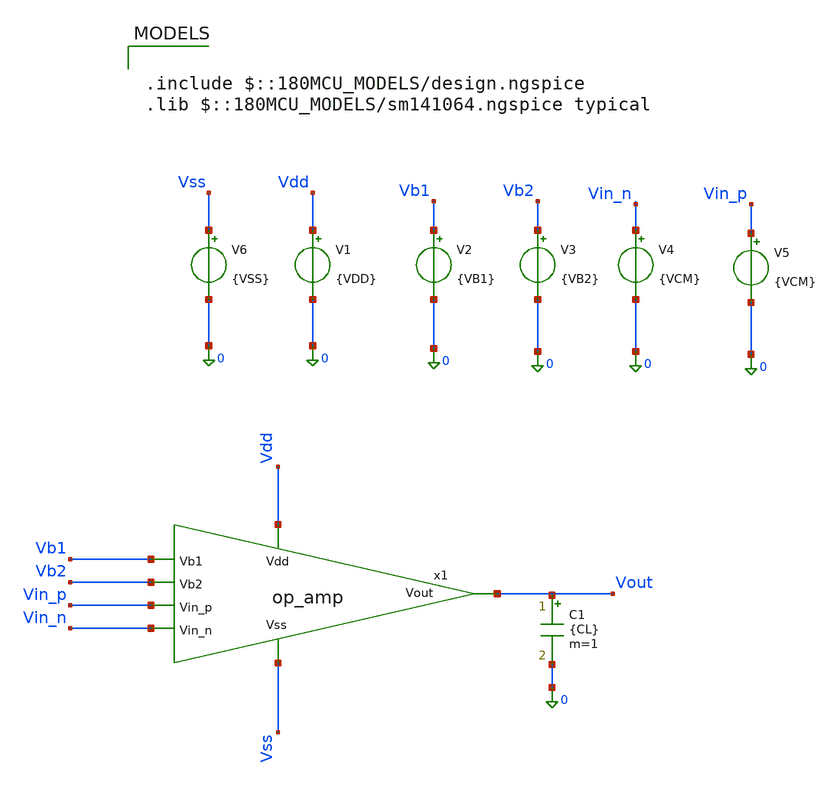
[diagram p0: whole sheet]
** sch_path: blocks/adc/lvds/ota_test.sch
**.subckt ota_test
C1 net1 0 {CL} m=1
V1 Vdd 0 {VDD}
V2 Vb1 0 {VB1}
V3 Vb2 0 {VB2}
V4 Vin_n 0 {VCM}
V5 Vin_p 0 {VCM}
x1 Vdd Vb1 Vout Vb2 Vin_p Vin_n Vss op_amp
V6 Vss 0 {VSS}
**** begin user architecture code


.param VDD=3.3
.param VSS=0
.param VCM=1.2
.param VB1=0
.param VB2=0
.param CL=100f

.control
save all
set wr_vecnames
set wr_singlescale

dc V2 0 2.5 0.01 V3 0 2.5 0.01

* XM1
let xm1_id    = @m.x1.xm1.m0[id]
let xm1_vgs   = @m.x1.xm1.m0[vgs]
let xm1_vds   = @m.x1.xm1.m0[vds]
let xm1_vth   = @m.x1.xm1.m0[vth]
let xm1_vdsat = @m.x1.xm1.m0[vdsat]
let xm1_gm    = @m.x1.xm1.m0[gm]
let xm1_gds   = @m.x1.xm1.m0[gds]

* XM2
let xm2_id    = @m.x1.xm2.m0[id]
let xm2_vgs   = @m.x1.xm2.m0[vgs]
let xm2_vds   = @m.x1.xm2.m0[vds]
let xm2_vth   = @m.x1.xm2.m0[vth]
let xm2_vdsat = @m.x1.xm2.m0[vdsat]
let xm2_gm    = @m.x1.xm2.m0[gm]
let xm2_gds   = @m.x1.xm2.m0[gds]

* XM3
let xm3_id    = @m.x1.xm3.m0[id]
let xm3_vgs   = @m.x1.xm3.m0[vgs]
let xm3_vds   = @m.x1.xm3.m0[vds]
let xm3_vth   = @m.x1.xm3.m0[vth]
let xm3_vdsat = @m.x1.xm3.m0[vdsat]
let xm3_gm    = @m.x1.xm3.m0[gm]
let xm3_gds   = @m.x1.xm3.m0[gds]

* XM4
let xm4_id    = @m.x1.xm4.m0[id]
let xm4_vgs   = @m.x1.xm4.m0[vgs]
let xm4_vds   = @m.x1.xm4.m0[vds]
let xm4_vth   = @m.x1.xm4.m0[vth]
let xm4_vdsat = @m.x1.xm4.m0[vdsat]
let xm4_gm    = @m.x1.xm4.m0[gm]
let xm4_gds   = @m.x1.xm4.m0[gds]

* XM5
let xm5_id    = @m.x1.xm5.m0[id]
let xm5_vgs   = @m.x1.xm5.m0[vgs]
let xm5_vds   = @m.x1.xm5.m0[vds]
let xm5_vth   = @m.x1.xm5.m0[vth]
let xm5_vdsat = @m.x1.xm5.m0[vdsat]
let xm5_gm    = @m.x1.xm5.m0[gm]
let xm5_gds   = @m.x1.xm5.m0[gds]

* XM6
let xm6_id    = @m.x1.xm6.m0[id]
let xm6_vgs   = @m.x1.xm6.m0[vgs]
let xm6_vds   = @m.x1.xm6.m0[vds]
let xm6_vth   = @m.x1.xm6.m0[vth]
let xm6_vdsat = @m.x1.xm6.m0[vdsat]
let xm6_gm    = @m.x1.xm6.m0[gm]
let xm6_gds   = @m.x1.xm6.m0[gds]

* XM7
let xm7_id    = @m.x1.xm7.m0[id]
let xm7_vgs   = @m.x1.xm7.m0[vgs]
let xm7_vds   = @m.x1.xm7.m0[vds]
let xm7_vth   = @m.x1.xm7.m0[vth]
let xm7_vdsat = @m.x1.xm7.m0[vdsat]
let xm7_gm    = @m.x1.xm7.m0[gm]
let xm7_gds   = @m.x1.xm7.m0[gds]

* XM8
let xm8_id    = @m.x1.xm8.m0[id]
let xm8_vgs   = @m.x1.xm8.m0[vgs]
let xm8_vds   = @m.x1.xm8.m0[vds]
let xm8_vth   = @m.x1.xm8.m0[vth]
let xm8_vdsat = @m.x1.xm8.m0[vdsat]
let xm8_gm    = @m.x1.xm8.m0[gm]
let xm8_gds   = @m.x1.xm8.m0[gds]

* XM9
let xm9_id    = @m.x1.xm9.m0[id]
let xm9_vgs   = @m.x1.xm9.m0[vgs]
let xm9_vds   = @m.x1.xm9.m0[vds]
let xm9_vth   = @m.x1.xm9.m0[vth]
let xm9_vdsat = @m.x1.xm9.m0[vdsat]
let xm9_gm    = @m.x1.xm9.m0[gm]
let xm9_gds   = @m.x1.xm9.m0[gds]

* XM10
let xm10_id    = @m.x1.xm10.m0[id]
let xm10_vgs   = @m.x1.xm10.m0[vgs]
let xm10_vds   = @m.x1.xm10.m0[vds]
let xm10_vth   = @m.x1.xm10.m0[vth]
let xm10_vdsat = @m.x1.xm10.m0[vdsat]
let xm10_gm    = @m.x1.xm10.m0[gm]
let xm10_gds   = @m.x1.xm10.m0[gds]

* XM11
let xm11_id    = @m.x1.xm11.m0[id]
let xm11_vgs   = @m.x1.xm11.m0[vgs]
let xm11_vds   = @m.x1.xm11.m0[vds]
let xm11_vth   = @m.x1.xm11.m0[vth]
let xm11_vdsat = @m.x1.xm11.m0[vdsat]
let xm11_gm    = @m.x1.xm11.m0[gm]
let xm11_gds   = @m.x1.xm11.m0[gds]

* XM12
let xm12_id    = @m.x1.xm12.m0[id]
let xm12_vgs   = @m.x1.xm12.m0[vgs]
let xm12_vds   = @m.x1.xm12.m0[vds]
let xm12_vth   = @m.x1.xm12.m0[vth]
let xm12_vdsat = @m.x1.xm12.m0[vdsat]
let xm12_gm    = @m.x1.xm12.m0[gm]
let xm12_gds   = @m.x1.xm12.m0[gds]

* XM13
let xm13_id    = @m.x1.xm13.m0[id]
let xm13_vgs   = @m.x1.xm13.m0[vgs]
let xm13_vds   = @m.x1.xm13.m0[vds]
let xm13_vth   = @m.x1.xm13.m0[vth]
let xm13_vdsat = @m.x1.xm13.m0[vdsat]
let xm13_gm    = @m.x1.xm13.m0[gm]
let xm13_gds   = @m.x1.xm13.m0[gds]

* XM14
let xm14_id    = @m.x1.xm14.m0[id]
let xm14_vgs   = @m.x1.xm14.m0[vgs]
let xm14_vds   = @m.x1.xm14.m0[vds]
let xm14_vth   = @m.x1.xm14.m0[vth]
let xm14_vdsat = @m.x1.xm14.m0[vdsat]
let xm14_gm    = @m.x1.xm14.m0[gm]
let xm14_gds   = @m.x1.xm14.m0[gds]

* Check that vectors exist
display

wrdata /foss/designs/trans_testing/ota_testing/ota_bias_device_data.txt v(vb1) v(vb2) v(vout) xm1_id
+ xm1_vgs xm1_vds xm1_vth xm1_vdsat xm1_gm xm1_gds xm2_id xm2_vgs xm2_vds xm2_vth xm2_vdsat xm2_gm xm2_gds
+ xm3_id xm3_vgs xm3_vds xm3_vth xm3_vdsat xm3_gm xm3_gds xm4_id xm4_vgs xm4_vds xm4_vth xm4_vdsat xm4_gm
+ xm4_gds xm5_id xm5_vgs xm5_vds xm5_vth xm5_vdsat xm5_gm xm5_gds xm6_id xm6_vgs xm6_vds xm6_vth xm6_vdsat
+ xm6_gm xm6_gds xm7_id xm7_vgs xm7_vds xm7_vth xm7_vdsat xm7_gm xm7_gds xm8_id xm8_vgs xm8_vds xm8_vth
+ xm8_vdsat xm8_gm xm8_gds xm9_id xm9_vgs xm9_vds xm9_vth xm9_vdsat xm9_gm xm9_gds xm10_id xm10_vgs xm10_vds
+ xm10_vth xm10_vdsat xm10_gm xm10_gds xm11_id xm11_vgs xm11_vds xm11_vth xm11_vdsat xm11_gm xm11_gds xm12_id
+ xm12_vgs xm12_vds xm12_vth xm12_vdsat xm12_gm xm12_gds xm13_id xm13_vgs xm13_vds xm13_vth xm13_vdsat xm13_gm
+ xm13_gds xm14_id xm14_vgs xm14_vds xm14_vth xm14_vdsat xm14_gm xm14_gds

.endc



.include $::180MCU_MODELS/design.ngspice
.lib $::180MCU_MODELS/sm141064.ngspice typical

**** end user architecture code
**.ends

* expanding   symbol:  op_amp.sym # of pins=7
** sym_path: blocks/adc/lvds/op_amp.sym
** sch_path: blocks/adc/lvds/op_amp.sch
.subckt op_amp Vdd Vb1 Vout Vb2 Vin_p Vin_n Vss
*.ipin Vdd
*.ipin Vb2
*.ipin Vin_p
*.ipin Vin_n
*.ipin Vb1
*.opin Vout
*.ipin Vss
XM1 VdM1 vgM1 Vdd Vdd pfet_03v3 L=0.28u W=10.5u nf=1 ad='int((nf+1)/2) * W/nf * 0.18u' as='int((nf+2)/2) * W/nf * 0.18u'
+ pd='2*int((nf+1)/2) * (W/nf + 0.18u)' ps='2*int((nf+2)/2) * (W/nf + 0.18u)' nrd='0.18u / W' nrs='0.18u / W'
+ sa=0 sb=0 sd=0 m=1
XM2 VdM2 VdM4 Vdd Vdd pfet_03v3 L=0.28u W=10.5u nf=1 ad='int((nf+1)/2) * W/nf * 0.18u' as='int((nf+2)/2) * W/nf * 0.18u'
+ pd='2*int((nf+1)/2) * (W/nf + 0.18u)' ps='2*int((nf+2)/2) * (W/nf + 0.18u)' nrd='0.18u / W' nrs='0.18u / W'
+ sa=0 sb=0 sd=0 m=1
XM3 vgM1 Vb2 VdM1 Vdd pfet_03v3 L=0.28u W=10.5u nf=1 ad='int((nf+1)/2) * W/nf * 0.18u' as='int((nf+2)/2) * W/nf * 0.18u'
+ pd='2*int((nf+1)/2) * (W/nf + 0.18u)' ps='2*int((nf+2)/2) * (W/nf + 0.18u)' nrd='0.18u / W' nrs='0.18u / W'
+ sa=0 sb=0 sd=0 m=1
XM4 VdM4 Vb2 VdM2 Vdd pfet_03v3 L=0.28u W=10.5u nf=1 ad='int((nf+1)/2) * W/nf * 0.18u' as='int((nf+2)/2) * W/nf * 0.18u'
+ pd='2*int((nf+1)/2) * (W/nf + 0.18u)' ps='2*int((nf+2)/2) * (W/nf + 0.18u)' nrd='0.18u / W' nrs='0.18u / W'
+ sa=0 sb=0 sd=0 m=1
XM5 VdM4 Vin_p VsM5 Vdd nfet_03v3 L=0.28u W=52.5u nf=15 ad='int((nf+1)/2) * W/nf * 0.18u' as='int((nf+2)/2) * W/nf * 0.18u'
+ pd='2*int((nf+1)/2) * (W/nf + 0.18u)' ps='2*int((nf+2)/2) * (W/nf + 0.18u)' nrd='0.18u / W' nrs='0.18u / W'
+ sa=0 sb=0 sd=0 m=1
XM6 vgM1 Vin_n VsM5 Vdd nfet_03v3 L=0.28u W=52.5u nf=15 ad='int((nf+1)/2) * W/nf * 0.18u' as='int((nf+2)/2) * W/nf * 0.18u'
+ pd='2*int((nf+1)/2) * (W/nf + 0.18u)' ps='2*int((nf+2)/2) * (W/nf + 0.18u)' nrd='0.18u / W' nrs='0.18u / W'
+ sa=0 sb=0 sd=0 m=1
XM7 VdM7 VdM4 Vdd Vdd pfet_03v3 L=0.28u W=10.5u nf=1 ad='int((nf+1)/2) * W/nf * 0.18u' as='int((nf+2)/2) * W/nf * 0.18u'
+ pd='2*int((nf+1)/2) * (W/nf + 0.18u)' ps='2*int((nf+2)/2) * (W/nf + 0.18u)' nrd='0.18u / W' nrs='0.18u / W'
+ sa=0 sb=0 sd=0 m=1
XM9 VdM9 vgM1 Vdd Vdd pfet_03v3 L=0.28u W=10.5u nf=1 ad='int((nf+1)/2) * W/nf * 0.18u' as='int((nf+2)/2) * W/nf * 0.18u'
+ pd='2*int((nf+1)/2) * (W/nf + 0.18u)' ps='2*int((nf+2)/2) * (W/nf + 0.18u)' nrd='0.18u / W' nrs='0.18u / W'
+ sa=0 sb=0 sd=0 m=1
XM11 VgM14 Vb2 net2 0 nfet_03v3 L=0.28u W=5.25u nf=1 ad='int((nf+1)/2) * W/nf * 0.18u' as='int((nf+2)/2) * W/nf * 0.18u'
+ pd='2*int((nf+1)/2) * (W/nf + 0.18u)' ps='2*int((nf+2)/2) * (W/nf + 0.18u)' nrd='0.18u / W' nrs='0.18u / W'
+ sa=0 sb=0 sd=0 m=1
XM12 Vout Vb2 net1 0 nfet_03v3 L=0.28u W=5.25u nf=1 ad='int((nf+1)/2) * W/nf * 0.18u' as='int((nf+2)/2) * W/nf * 0.18u'
+ pd='2*int((nf+1)/2) * (W/nf + 0.18u)' ps='2*int((nf+2)/2) * (W/nf + 0.18u)' nrd='0.18u / W' nrs='0.18u / W'
+ sa=0 sb=0 sd=0 m=1
XM13 net2 VgM14 0 0 nfet_03v3 L=0.28u W=5.25u nf=1 ad='int((nf+1)/2) * W/nf * 0.18u' as='int((nf+2)/2) * W/nf * 0.18u'
+ pd='2*int((nf+1)/2) * (W/nf + 0.18u)' ps='2*int((nf+2)/2) * (W/nf + 0.18u)' nrd='0.18u / W' nrs='0.18u / W'
+ sa=0 sb=0 sd=0 m=1
XM14 net1 VgM14 0 0 nfet_03v3 L=0.28u W=5.25u nf=1 ad='int((nf+1)/2) * W/nf * 0.18u' as='int((nf+2)/2) * W/nf * 0.18u'
+ pd='2*int((nf+1)/2) * (W/nf + 0.18u)' ps='2*int((nf+2)/2) * (W/nf + 0.18u)' nrd='0.18u / W' nrs='0.18u / W'
+ sa=0 sb=0 sd=0 m=1
ibias VsM5 Vss 250u
XM8 VgM14 Vb1 VdM7 Vdd pfet_03v3 L=0.28u W=10.5u nf=1 ad='int((nf+1)/2) * W/nf * 0.18u' as='int((nf+2)/2) * W/nf * 0.18u'
+ pd='2*int((nf+1)/2) * (W/nf + 0.18u)' ps='2*int((nf+2)/2) * (W/nf + 0.18u)' nrd='0.18u / W' nrs='0.18u / W'
+ sa=0 sb=0 sd=0 m=1
XM10 Vout Vb1 VdM9 Vdd pfet_03v3 L=0.28u W=10.5u nf=1 ad='int((nf+1)/2) * W/nf * 0.18u' as='int((nf+2)/2) * W/nf * 0.18u'
+ pd='2*int((nf+1)/2) * (W/nf + 0.18u)' ps='2*int((nf+2)/2) * (W/nf + 0.18u)' nrd='0.18u / W' nrs='0.18u / W'
+ sa=0 sb=0 sd=0 m=1
.ends

.end
